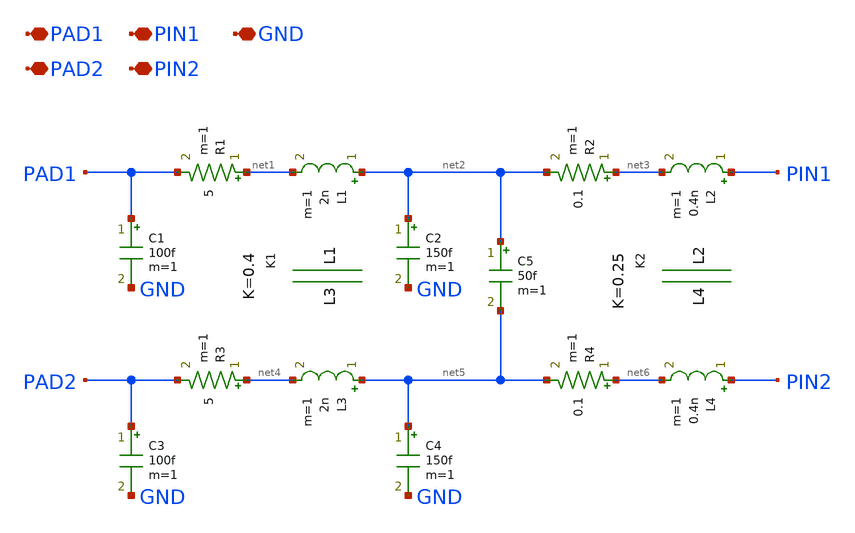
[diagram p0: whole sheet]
** sch_path: xschem/package_model.sch
**.subckt package_model PAD1 PAD2 PIN1 PIN2 GND
*.iopin PAD1
*.iopin PAD2
*.iopin PIN1
*.iopin PIN2
*.iopin GND
C1 PAD1 GND 100f m=1
R1 net1 PAD1 5 m=1
L1 net2 net1 2n m=1
C2 net2 GND 150f m=1
R2 net3 net2 0.1 m=1
L2 PIN1 net3 0.4n m=1
C5 net2 net5 50f m=1
K1 L1 L3 0.4
K2 L2 L4 0.25
C3 PAD2 GND 100f m=1
R3 net4 PAD2 5 m=1
L3 net5 net4 2n m=1
C4 net5 GND 150f m=1
R4 net6 net5 0.1 m=1
L4 PIN2 net6 0.4n m=1
**.ends
.end
